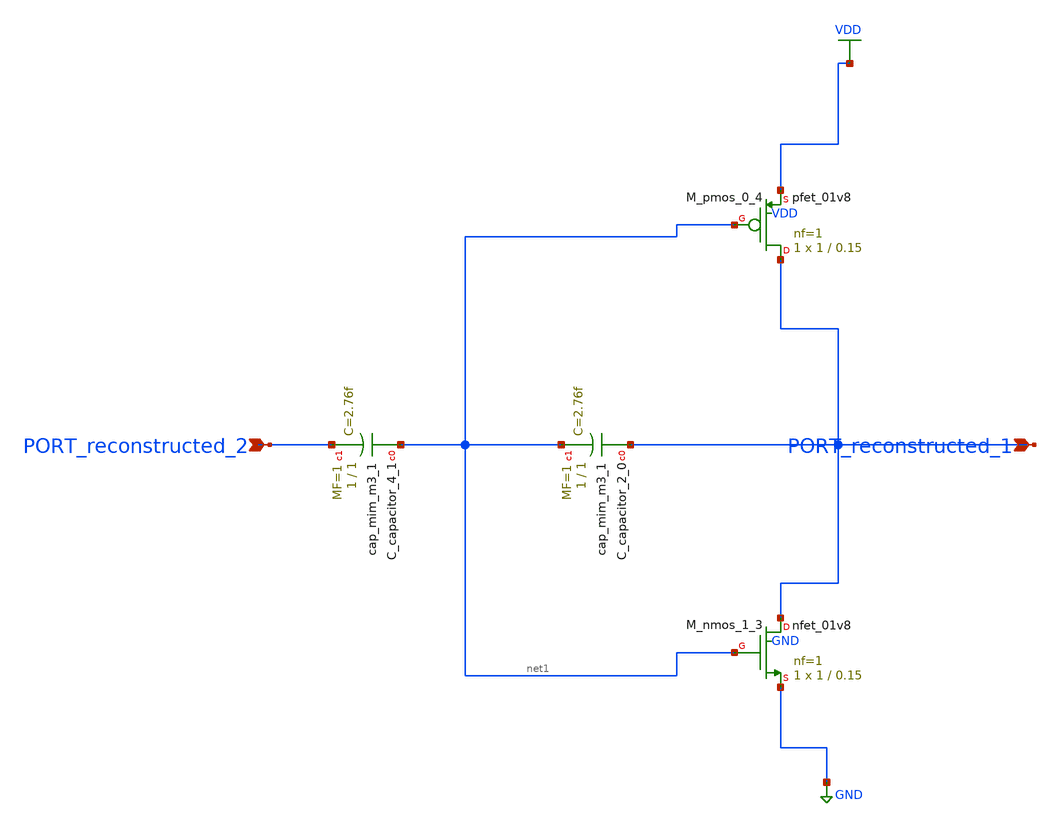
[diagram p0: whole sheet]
** sch_path: schematics/AMSNet/417.sch
**.subckt 417 PORT_reconstructed_2 PORT_reconstructed_1
*.ipin PORT_reconstructed_2
*.ipin PORT_reconstructed_1
XC_capacitor_2_0 PORT_reconstructed_1 net1 sky130_fd_pr__cap_mim_m3_1 W=1 L=1 MF=1 m=1
XC_capacitor_4_1 net1 PORT_reconstructed_2 sky130_fd_pr__cap_mim_m3_1 W=1 L=1 MF=1 m=1
XM_nmos_1_3 PORT_reconstructed_1 net1 GND GND sky130_fd_pr__nfet_01v8 L=0.15 W=1 nf=1 ad='int((1 + 1)/2) * 1 / 1 * 0.29'
+ as='int((1 + 2)/2) * 1 / 1 * 0.29' pd='2*int((1 + 1)/2) * (1 / 1 + 0.29)' ps='2*int((1 + 2)/2) * (1 / 1 + 0.29)'
+ nrd='0.29 / 1 ' nrs='0.29 / 1 ' sa=0 sb=0 sd=0 mult=1 m=1
XM_pmos_0_4 PORT_reconstructed_1 net1 VDD VDD sky130_fd_pr__pfet_01v8 L=0.15 W=1 nf=1 ad='int((1 + 1)/2) * 1 / 1 * 0.29'
+ as='int((1 + 2)/2) * 1 / 1 * 0.29' pd='2*int((1 + 1)/2) * (1 / 1 + 0.29)' ps='2*int((1 + 2)/2) * (1 / 1 + 0.29)'
+ nrd='0.29 / 1 ' nrs='0.29 / 1 ' sa=0 sb=0 sd=0 mult=1 m=1
**.ends
.GLOBAL GND
.GLOBAL VDD
.end
